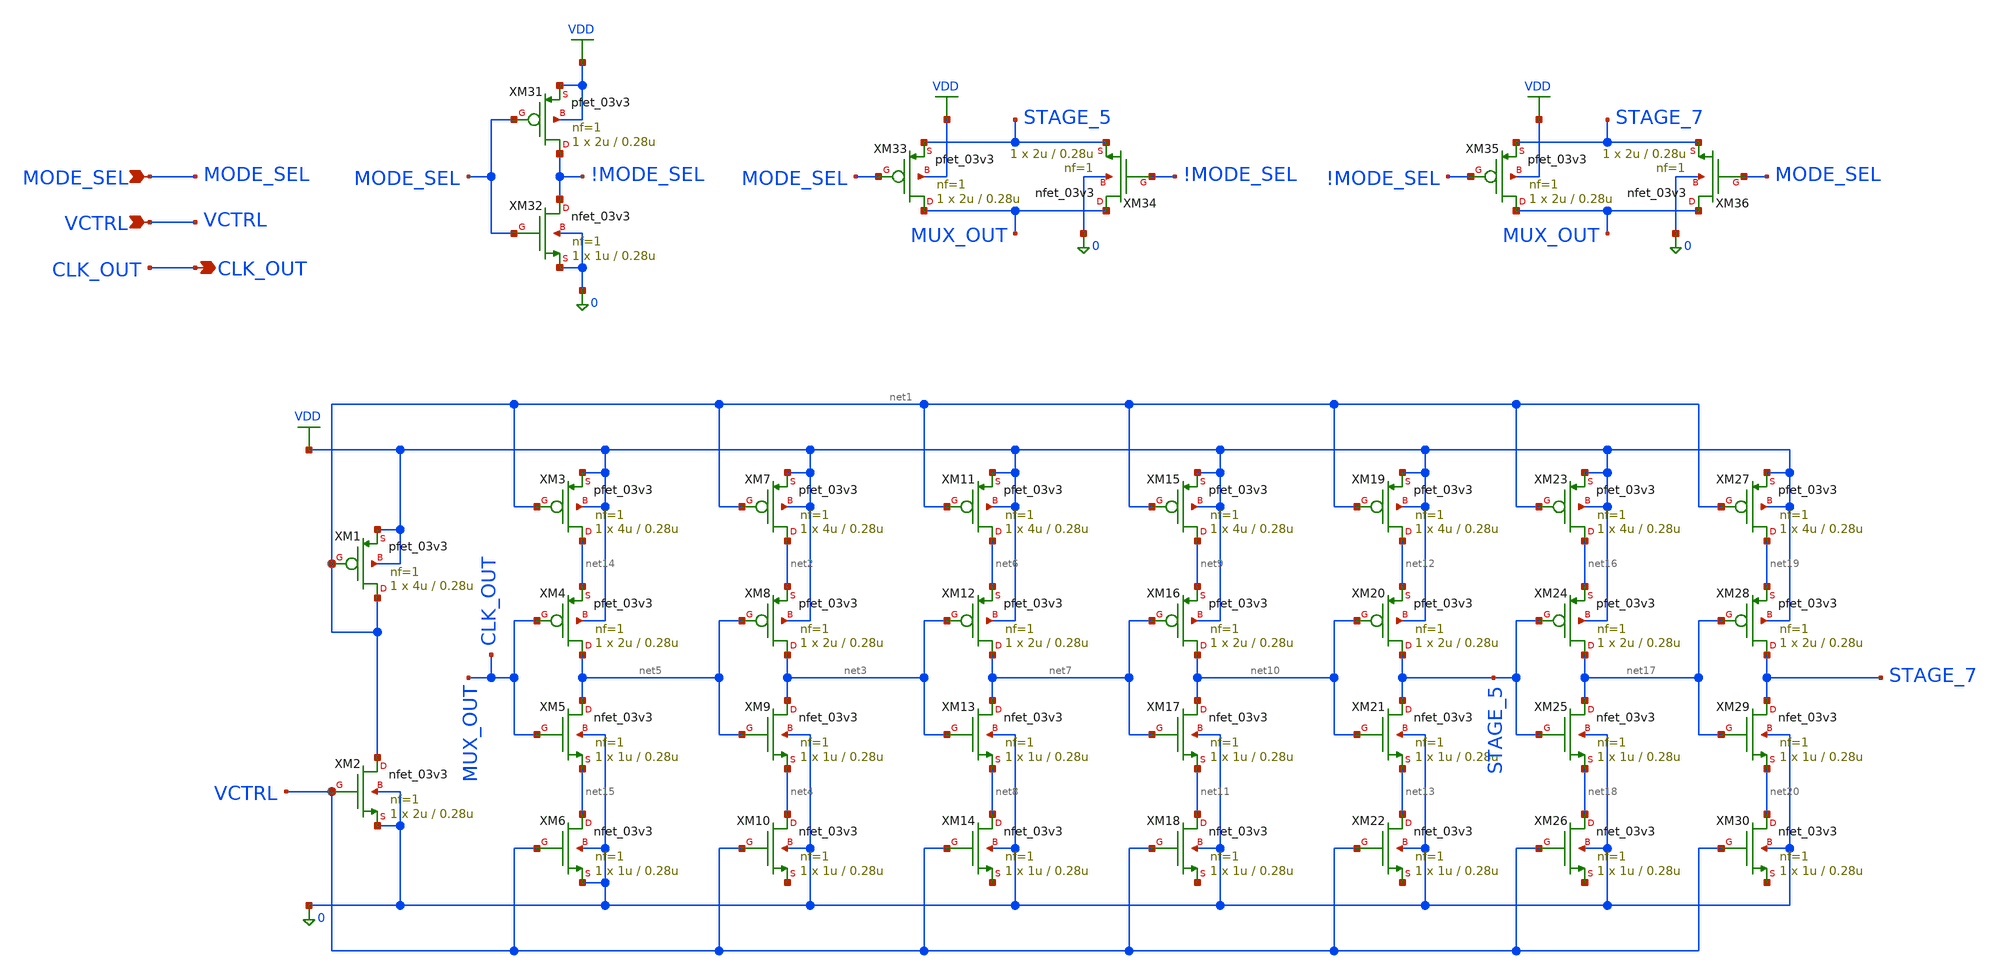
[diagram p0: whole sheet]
** sch_path: src/Ring_VCO/ring_VCO.sch
**.subckt ring_VCO VCTRL CLK_OUT MODE_SEL
*.ipin VCTRL
*.opin CLK_OUT
*.ipin MODE_SEL
XM1 net1 net1 VDD VDD pfet_03v3 L=0.28u W=4u nf=1 ad='int((nf+1)/2) * W/nf * 0.18u' as='int((nf+2)/2) * W/nf * 0.18u'
+ pd='2*int((nf+1)/2) * (W/nf + 0.18u)' ps='2*int((nf+2)/2) * (W/nf + 0.18u)' nrd='0.18u / W' nrs='0.18u / W'
+ sa=0 sb=0 sd=0 m=1
XM2 net1 VCTRL 0 0 nfet_03v3 L=0.28u W=2u nf=1 ad='int((nf+1)/2) * W/nf * 0.18u' as='int((nf+2)/2) * W/nf * 0.18u'
+ pd='2*int((nf+1)/2) * (W/nf + 0.18u)' ps='2*int((nf+2)/2) * (W/nf + 0.18u)' nrd='0.18u / W' nrs='0.18u / W'
+ sa=0 sb=0 sd=0 m=1
XM3 net14 net1 VDD VDD pfet_03v3 L=0.28u W=4u nf=1 ad='int((nf+1)/2) * W/nf * 0.18u' as='int((nf+2)/2) * W/nf * 0.18u'
+ pd='2*int((nf+1)/2) * (W/nf + 0.18u)' ps='2*int((nf+2)/2) * (W/nf + 0.18u)' nrd='0.18u / W' nrs='0.18u / W'
+ sa=0 sb=0 sd=0 m=1
XM4 net5 MUX_OUT net14 VDD pfet_03v3 L=0.28u W=2u nf=1 ad='int((nf+1)/2) * W/nf * 0.18u' as='int((nf+2)/2) * W/nf * 0.18u'
+ pd='2*int((nf+1)/2) * (W/nf + 0.18u)' ps='2*int((nf+2)/2) * (W/nf + 0.18u)' nrd='0.18u / W' nrs='0.18u / W'
+ sa=0 sb=0 sd=0 m=1
XM5 net5 MUX_OUT net15 0 nfet_03v3 L=0.28u W=1u nf=1 ad='int((nf+1)/2) * W/nf * 0.18u' as='int((nf+2)/2) * W/nf * 0.18u'
+ pd='2*int((nf+1)/2) * (W/nf + 0.18u)' ps='2*int((nf+2)/2) * (W/nf + 0.18u)' nrd='0.18u / W' nrs='0.18u / W'
+ sa=0 sb=0 sd=0 m=1
XM6 net15 VCTRL 0 0 nfet_03v3 L=0.28u W=1u nf=1 ad='int((nf+1)/2) * W/nf * 0.18u' as='int((nf+2)/2) * W/nf * 0.18u'
+ pd='2*int((nf+1)/2) * (W/nf + 0.18u)' ps='2*int((nf+2)/2) * (W/nf + 0.18u)' nrd='0.18u / W' nrs='0.18u / W'
+ sa=0 sb=0 sd=0 m=1
XM7 net2 net1 VDD VDD pfet_03v3 L=0.28u W=4u nf=1 ad='int((nf+1)/2) * W/nf * 0.18u' as='int((nf+2)/2) * W/nf * 0.18u'
+ pd='2*int((nf+1)/2) * (W/nf + 0.18u)' ps='2*int((nf+2)/2) * (W/nf + 0.18u)' nrd='0.18u / W' nrs='0.18u / W'
+ sa=0 sb=0 sd=0 m=1
XM8 net3 net5 net2 VDD pfet_03v3 L=0.28u W=2u nf=1 ad='int((nf+1)/2) * W/nf * 0.18u' as='int((nf+2)/2) * W/nf * 0.18u'
+ pd='2*int((nf+1)/2) * (W/nf + 0.18u)' ps='2*int((nf+2)/2) * (W/nf + 0.18u)' nrd='0.18u / W' nrs='0.18u / W'
+ sa=0 sb=0 sd=0 m=1
XM9 net3 net5 net4 0 nfet_03v3 L=0.28u W=1u nf=1 ad='int((nf+1)/2) * W/nf * 0.18u' as='int((nf+2)/2) * W/nf * 0.18u'
+ pd='2*int((nf+1)/2) * (W/nf + 0.18u)' ps='2*int((nf+2)/2) * (W/nf + 0.18u)' nrd='0.18u / W' nrs='0.18u / W'
+ sa=0 sb=0 sd=0 m=1
XM10 net4 VCTRL net21 0 nfet_03v3 L=0.28u W=1u nf=1 ad='int((nf+1)/2) * W/nf * 0.18u' as='int((nf+2)/2) * W/nf * 0.18u'
+ pd='2*int((nf+1)/2) * (W/nf + 0.18u)' ps='2*int((nf+2)/2) * (W/nf + 0.18u)' nrd='0.18u / W' nrs='0.18u / W'
+ sa=0 sb=0 sd=0 m=1
XM11 net6 net1 VDD VDD pfet_03v3 L=0.28u W=4u nf=1 ad='int((nf+1)/2) * W/nf * 0.18u' as='int((nf+2)/2) * W/nf * 0.18u'
+ pd='2*int((nf+1)/2) * (W/nf + 0.18u)' ps='2*int((nf+2)/2) * (W/nf + 0.18u)' nrd='0.18u / W' nrs='0.18u / W'
+ sa=0 sb=0 sd=0 m=1
XM12 net7 net3 net6 VDD pfet_03v3 L=0.28u W=2u nf=1 ad='int((nf+1)/2) * W/nf * 0.18u' as='int((nf+2)/2) * W/nf * 0.18u'
+ pd='2*int((nf+1)/2) * (W/nf + 0.18u)' ps='2*int((nf+2)/2) * (W/nf + 0.18u)' nrd='0.18u / W' nrs='0.18u / W'
+ sa=0 sb=0 sd=0 m=1
XM13 net7 net3 net8 0 nfet_03v3 L=0.28u W=1u nf=1 ad='int((nf+1)/2) * W/nf * 0.18u' as='int((nf+2)/2) * W/nf * 0.18u'
+ pd='2*int((nf+1)/2) * (W/nf + 0.18u)' ps='2*int((nf+2)/2) * (W/nf + 0.18u)' nrd='0.18u / W' nrs='0.18u / W'
+ sa=0 sb=0 sd=0 m=1
XM14 net8 VCTRL net22 0 nfet_03v3 L=0.28u W=1u nf=1 ad='int((nf+1)/2) * W/nf * 0.18u' as='int((nf+2)/2) * W/nf * 0.18u'
+ pd='2*int((nf+1)/2) * (W/nf + 0.18u)' ps='2*int((nf+2)/2) * (W/nf + 0.18u)' nrd='0.18u / W' nrs='0.18u / W'
+ sa=0 sb=0 sd=0 m=1
XM15 net9 net1 VDD VDD pfet_03v3 L=0.28u W=4u nf=1 ad='int((nf+1)/2) * W/nf * 0.18u' as='int((nf+2)/2) * W/nf * 0.18u'
+ pd='2*int((nf+1)/2) * (W/nf + 0.18u)' ps='2*int((nf+2)/2) * (W/nf + 0.18u)' nrd='0.18u / W' nrs='0.18u / W'
+ sa=0 sb=0 sd=0 m=1
XM16 net10 net7 net9 VDD pfet_03v3 L=0.28u W=2u nf=1 ad='int((nf+1)/2) * W/nf * 0.18u' as='int((nf+2)/2) * W/nf * 0.18u'
+ pd='2*int((nf+1)/2) * (W/nf + 0.18u)' ps='2*int((nf+2)/2) * (W/nf + 0.18u)' nrd='0.18u / W' nrs='0.18u / W'
+ sa=0 sb=0 sd=0 m=1
XM17 net10 net7 net11 0 nfet_03v3 L=0.28u W=1u nf=1 ad='int((nf+1)/2) * W/nf * 0.18u' as='int((nf+2)/2) * W/nf * 0.18u'
+ pd='2*int((nf+1)/2) * (W/nf + 0.18u)' ps='2*int((nf+2)/2) * (W/nf + 0.18u)' nrd='0.18u / W' nrs='0.18u / W'
+ sa=0 sb=0 sd=0 m=1
XM18 net11 VCTRL net23 0 nfet_03v3 L=0.28u W=1u nf=1 ad='int((nf+1)/2) * W/nf * 0.18u' as='int((nf+2)/2) * W/nf * 0.18u'
+ pd='2*int((nf+1)/2) * (W/nf + 0.18u)' ps='2*int((nf+2)/2) * (W/nf + 0.18u)' nrd='0.18u / W' nrs='0.18u / W'
+ sa=0 sb=0 sd=0 m=1
XM19 net12 net1 VDD VDD pfet_03v3 L=0.28u W=4u nf=1 ad='int((nf+1)/2) * W/nf * 0.18u' as='int((nf+2)/2) * W/nf * 0.18u'
+ pd='2*int((nf+1)/2) * (W/nf + 0.18u)' ps='2*int((nf+2)/2) * (W/nf + 0.18u)' nrd='0.18u / W' nrs='0.18u / W'
+ sa=0 sb=0 sd=0 m=1
XM20 STAGE_5 net10 net12 VDD pfet_03v3 L=0.28u W=2u nf=1 ad='int((nf+1)/2) * W/nf * 0.18u' as='int((nf+2)/2) * W/nf * 0.18u'
+ pd='2*int((nf+1)/2) * (W/nf + 0.18u)' ps='2*int((nf+2)/2) * (W/nf + 0.18u)' nrd='0.18u / W' nrs='0.18u / W'
+ sa=0 sb=0 sd=0 m=1
XM21 STAGE_5 net10 net13 0 nfet_03v3 L=0.28u W=1u nf=1 ad='int((nf+1)/2) * W/nf * 0.18u' as='int((nf+2)/2) * W/nf * 0.18u'
+ pd='2*int((nf+1)/2) * (W/nf + 0.18u)' ps='2*int((nf+2)/2) * (W/nf + 0.18u)' nrd='0.18u / W' nrs='0.18u / W'
+ sa=0 sb=0 sd=0 m=1
XM22 net13 VCTRL net24 0 nfet_03v3 L=0.28u W=1u nf=1 ad='int((nf+1)/2) * W/nf * 0.18u' as='int((nf+2)/2) * W/nf * 0.18u'
+ pd='2*int((nf+1)/2) * (W/nf + 0.18u)' ps='2*int((nf+2)/2) * (W/nf + 0.18u)' nrd='0.18u / W' nrs='0.18u / W'
+ sa=0 sb=0 sd=0 m=1
XM23 net16 net1 VDD VDD pfet_03v3 L=0.28u W=4u nf=1 ad='int((nf+1)/2) * W/nf * 0.18u' as='int((nf+2)/2) * W/nf * 0.18u'
+ pd='2*int((nf+1)/2) * (W/nf + 0.18u)' ps='2*int((nf+2)/2) * (W/nf + 0.18u)' nrd='0.18u / W' nrs='0.18u / W'
+ sa=0 sb=0 sd=0 m=1
XM24 net17 STAGE_5 net16 VDD pfet_03v3 L=0.28u W=2u nf=1 ad='int((nf+1)/2) * W/nf * 0.18u' as='int((nf+2)/2) * W/nf * 0.18u'
+ pd='2*int((nf+1)/2) * (W/nf + 0.18u)' ps='2*int((nf+2)/2) * (W/nf + 0.18u)' nrd='0.18u / W' nrs='0.18u / W'
+ sa=0 sb=0 sd=0 m=1
XM25 net17 STAGE_5 net18 0 nfet_03v3 L=0.28u W=1u nf=1 ad='int((nf+1)/2) * W/nf * 0.18u' as='int((nf+2)/2) * W/nf * 0.18u'
+ pd='2*int((nf+1)/2) * (W/nf + 0.18u)' ps='2*int((nf+2)/2) * (W/nf + 0.18u)' nrd='0.18u / W' nrs='0.18u / W'
+ sa=0 sb=0 sd=0 m=1
XM26 net18 VCTRL net25 0 nfet_03v3 L=0.28u W=1u nf=1 ad='int((nf+1)/2) * W/nf * 0.18u' as='int((nf+2)/2) * W/nf * 0.18u'
+ pd='2*int((nf+1)/2) * (W/nf + 0.18u)' ps='2*int((nf+2)/2) * (W/nf + 0.18u)' nrd='0.18u / W' nrs='0.18u / W'
+ sa=0 sb=0 sd=0 m=1
XM27 net19 net1 VDD VDD pfet_03v3 L=0.28u W=4u nf=1 ad='int((nf+1)/2) * W/nf * 0.18u' as='int((nf+2)/2) * W/nf * 0.18u'
+ pd='2*int((nf+1)/2) * (W/nf + 0.18u)' ps='2*int((nf+2)/2) * (W/nf + 0.18u)' nrd='0.18u / W' nrs='0.18u / W'
+ sa=0 sb=0 sd=0 m=1
XM28 STAGE_7 net17 net19 VDD pfet_03v3 L=0.28u W=2u nf=1 ad='int((nf+1)/2) * W/nf * 0.18u' as='int((nf+2)/2) * W/nf * 0.18u'
+ pd='2*int((nf+1)/2) * (W/nf + 0.18u)' ps='2*int((nf+2)/2) * (W/nf + 0.18u)' nrd='0.18u / W' nrs='0.18u / W'
+ sa=0 sb=0 sd=0 m=1
XM29 STAGE_7 net17 net20 0 nfet_03v3 L=0.28u W=1u nf=1 ad='int((nf+1)/2) * W/nf * 0.18u' as='int((nf+2)/2) * W/nf * 0.18u'
+ pd='2*int((nf+1)/2) * (W/nf + 0.18u)' ps='2*int((nf+2)/2) * (W/nf + 0.18u)' nrd='0.18u / W' nrs='0.18u / W'
+ sa=0 sb=0 sd=0 m=1
XM30 net20 VCTRL net26 0 nfet_03v3 L=0.28u W=1u nf=1 ad='int((nf+1)/2) * W/nf * 0.18u' as='int((nf+2)/2) * W/nf * 0.18u'
+ pd='2*int((nf+1)/2) * (W/nf + 0.18u)' ps='2*int((nf+2)/2) * (W/nf + 0.18u)' nrd='0.18u / W' nrs='0.18u / W'
+ sa=0 sb=0 sd=0 m=1
XM31 !MODE_SEL MODE_SEL VDD VDD pfet_03v3 L=0.28u W=2u nf=1 ad='int((nf+1)/2) * W/nf * 0.18u' as='int((nf+2)/2) * W/nf * 0.18u'
+ pd='2*int((nf+1)/2) * (W/nf + 0.18u)' ps='2*int((nf+2)/2) * (W/nf + 0.18u)' nrd='0.18u / W' nrs='0.18u / W'
+ sa=0 sb=0 sd=0 m=1
XM32 !MODE_SEL MODE_SEL 0 0 nfet_03v3 L=0.28u W=1u nf=1 ad='int((nf+1)/2) * W/nf * 0.18u' as='int((nf+2)/2) * W/nf * 0.18u'
+ pd='2*int((nf+1)/2) * (W/nf + 0.18u)' ps='2*int((nf+2)/2) * (W/nf + 0.18u)' nrd='0.18u / W' nrs='0.18u / W'
+ sa=0 sb=0 sd=0 m=1
XM33 MUX_OUT MODE_SEL STAGE_5 VDD pfet_03v3 L=0.28u W=2u nf=1 ad='int((nf+1)/2) * W/nf * 0.18u' as='int((nf+2)/2) * W/nf * 0.18u'
+ pd='2*int((nf+1)/2) * (W/nf + 0.18u)' ps='2*int((nf+2)/2) * (W/nf + 0.18u)' nrd='0.18u / W' nrs='0.18u / W'
+ sa=0 sb=0 sd=0 m=1
XM34 MUX_OUT !MODE_SEL STAGE_5 0 nfet_03v3 L=0.28u W=2u nf=1 ad='int((nf+1)/2) * W/nf * 0.18u' as='int((nf+2)/2) * W/nf * 0.18u'
+ pd='2*int((nf+1)/2) * (W/nf + 0.18u)' ps='2*int((nf+2)/2) * (W/nf + 0.18u)' nrd='0.18u / W' nrs='0.18u / W'
+ sa=0 sb=0 sd=0 m=1
XM35 MUX_OUT !MODE_SEL STAGE_7 VDD pfet_03v3 L=0.28u W=2u nf=1 ad='int((nf+1)/2) * W/nf * 0.18u' as='int((nf+2)/2) * W/nf * 0.18u'
+ pd='2*int((nf+1)/2) * (W/nf + 0.18u)' ps='2*int((nf+2)/2) * (W/nf + 0.18u)' nrd='0.18u / W' nrs='0.18u / W'
+ sa=0 sb=0 sd=0 m=1
XM36 MUX_OUT MODE_SEL STAGE_7 0 nfet_03v3 L=0.28u W=2u nf=1 ad='int((nf+1)/2) * W/nf * 0.18u' as='int((nf+2)/2) * W/nf * 0.18u'
+ pd='2*int((nf+1)/2) * (W/nf + 0.18u)' ps='2*int((nf+2)/2) * (W/nf + 0.18u)' nrd='0.18u / W' nrs='0.18u / W'
+ sa=0 sb=0 sd=0 m=1
**.ends
.GLOBAL VDD
.end
